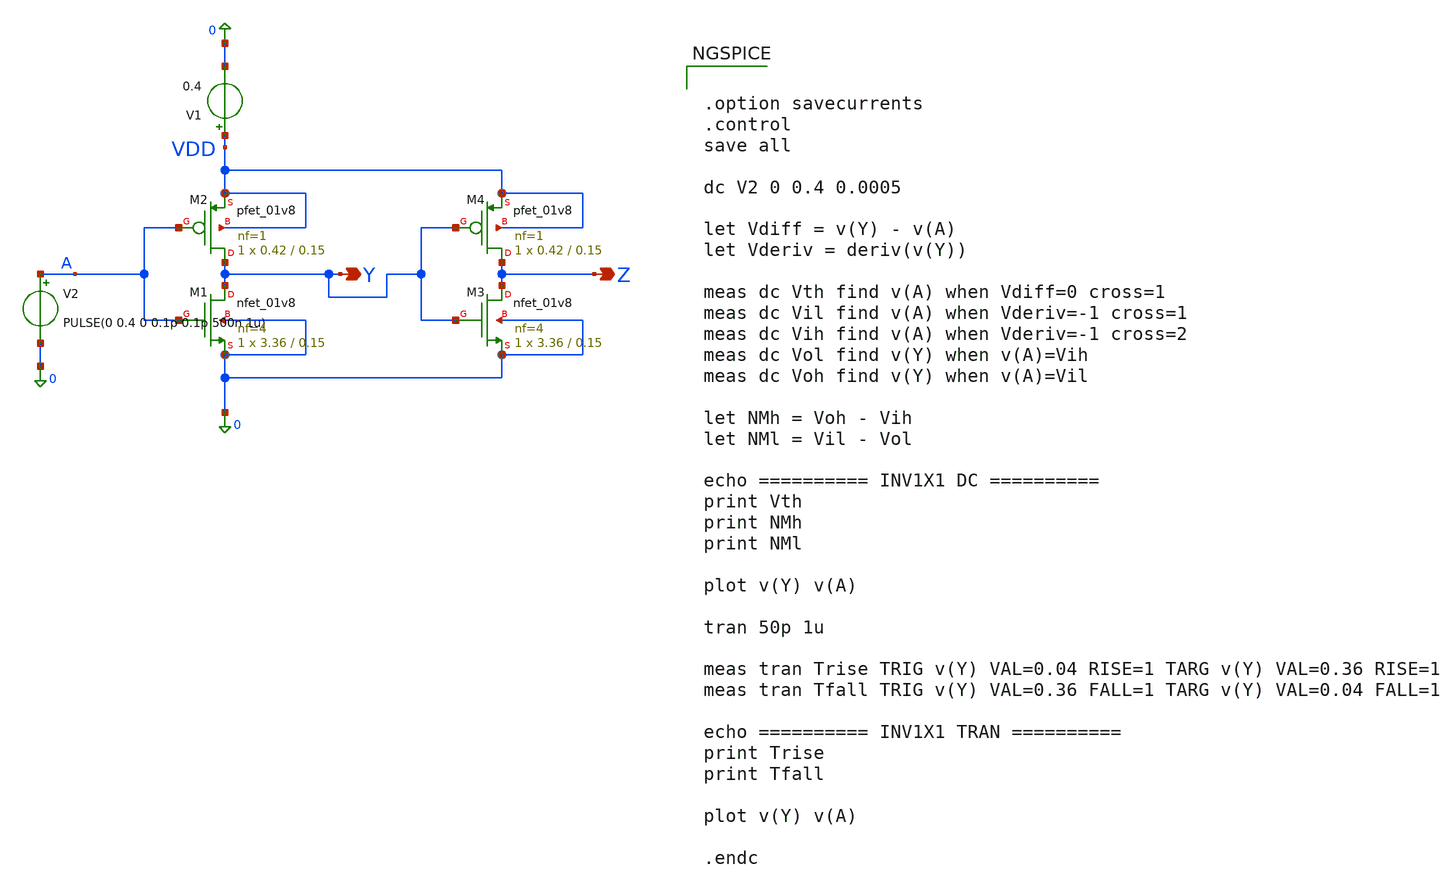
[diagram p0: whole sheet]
** sch_path: analysis/mep/mep_tb.sch
**.subckt mep_tb Y Z
*.opin Y
*.opin Z
V2 A 0 PULSE(0 0.4 0 0.1p 0.1p 500n 1u)
V1 VDD 0 0.4
XM1 Y A 0 0 sky130_fd_pr__nfet_01v8 L=0.15 W=3.36 nf=4 ad='int((4 + 1)/2) * 3.36 / 4 * 0.29' as='int((4 + 2)/2) * 3.36 / 4 * 0.29'
+ pd='2*int((4 + 1)/2) * (3.36 / 4 + 0.29)' ps='2*int((4 + 2)/2) * (3.36 / 4 + 0.29)' nrd='0.29 / 3.36 '
+ nrs='0.29 / 3.36 ' sa=0 sb=0 sd=0 mult=1 m=1
XM2 Y A VDD VDD sky130_fd_pr__pfet_01v8 L=0.15 W=0.42 nf=1 ad='int((1 + 1)/2) * 0.42 / 1 * 0.29' as='int((1 + 2)/2) * 0.42 / 1 * 0.29'
+ pd='2*int((1 + 1)/2) * (0.42 / 1 + 0.29)' ps='2*int((1 + 2)/2) * (0.42 / 1 + 0.29)' nrd='0.29 / 0.42 '
+ nrs='0.29 / 0.42 ' sa=0 sb=0 sd=0 mult=1 m=1
XM3 Z Y 0 0 sky130_fd_pr__nfet_01v8 L=0.15 W=3.36 nf=4 ad='int((4 + 1)/2) * 3.36 / 4 * 0.29' as='int((4 + 2)/2) * 3.36 / 4 * 0.29'
+ pd='2*int((4 + 1)/2) * (3.36 / 4 + 0.29)' ps='2*int((4 + 2)/2) * (3.36 / 4 + 0.29)' nrd='0.29 / 3.36 '
+ nrs='0.29 / 3.36 ' sa=0 sb=0 sd=0 mult=1 m=1
XM4 Z Y VDD VDD sky130_fd_pr__pfet_01v8 L=0.15 W=0.42 nf=1 ad='int((1 + 1)/2) * 0.42 / 1 * 0.29' as='int((1 + 2)/2) * 0.42 / 1 * 0.29'
+ pd='2*int((1 + 1)/2) * (0.42 / 1 + 0.29)' ps='2*int((1 + 2)/2) * (0.42 / 1 + 0.29)' nrd='0.29 / 0.42 '
+ nrs='0.29 / 0.42 ' sa=0 sb=0 sd=0 mult=1 m=1
**** begin user architecture code

** opencircuitdesign pdks install
.lib $::SKYWATER_MODELS/sky130.lib.spice tt



.option savecurrents
.control
save all

dc V2 0 0.4 0.0005

let Vdiff = v(Y) - v(A)
let Vderiv = deriv(v(Y))

meas dc Vth find v(A) when Vdiff=0 cross=1
meas dc Vil find v(A) when Vderiv=-1 cross=1
meas dc Vih find v(A) when Vderiv=-1 cross=2
meas dc Vol find v(Y) when v(A)=Vih
meas dc Voh find v(Y) when v(A)=Vil

let NMh = Voh - Vih
let NMl = Vil - Vol

echo ========== INV1X1 DC ==========
print Vth
print NMh
print NMl

plot v(Y) v(A)

tran 50p 1u

meas tran Trise TRIG v(Y) VAL=0.04 RISE=1 TARG v(Y) VAL=0.36 RISE=1
meas tran Tfall TRIG v(Y) VAL=0.36 FALL=1 TARG v(Y) VAL=0.04 FALL=1

echo ========== INV1X1 TRAN ==========
print Trise
print Tfall

plot v(Y) v(A)

.endc


**** end user architecture code
**.ends
.end
